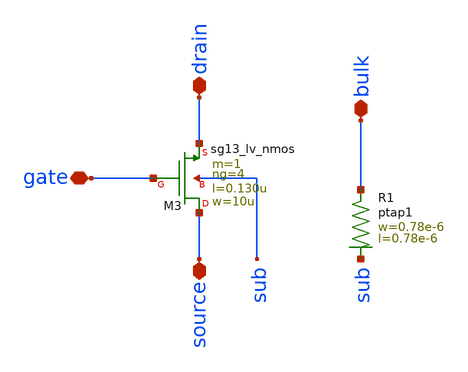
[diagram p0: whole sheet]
** sch_path: ts_pr_May2024/design_data/xschem/nmos4.sch
**.subckt nmos4 drain source bulk gate
*.iopin drain
*.iopin source
*.iopin bulk
*.iopin gate
XR1 bulk sub ptap1 R=262.8 w=0.78e-6 l=0.78e-6
XM3 source gate drain sub sg13_lv_nmos w=10u l=0.130u ng=4 m=1 mm_ok=1
**.ends
.end
